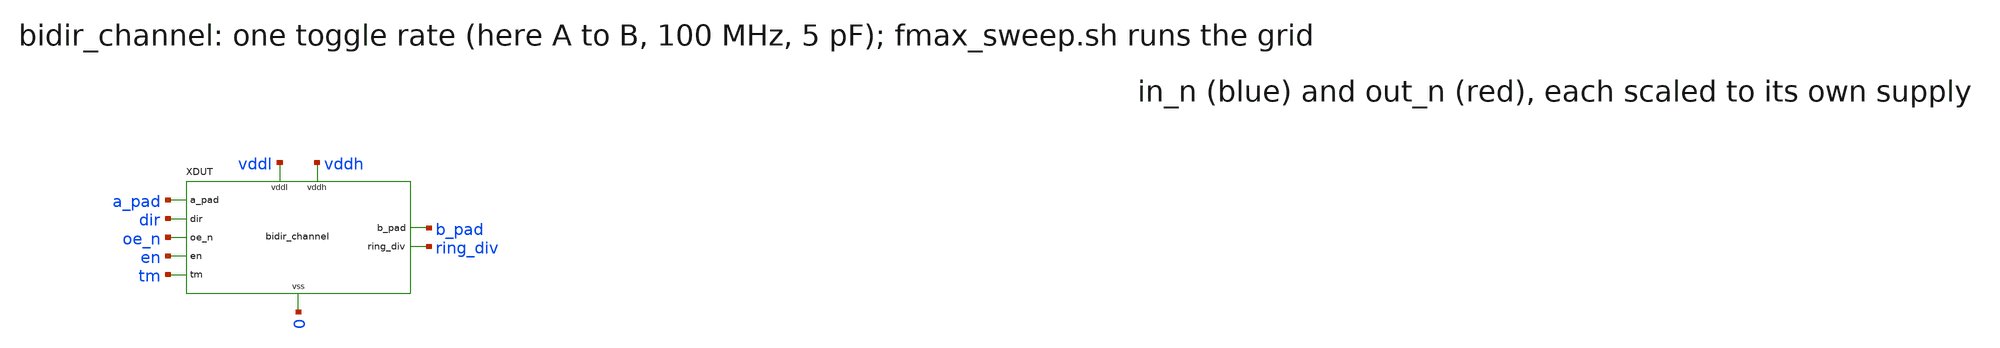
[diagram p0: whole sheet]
** sch_path: verification/tb_bidir_fmax.sch
**.subckt tb_bidir_fmax
XDUT a_pad b_pad dir oe_n en tm ring_div vddl vddh 0 bidir_channel
**** begin user architecture code

.lib cornerMOSlv.lib mos_tt
.lib cornerMOShv.lib mos_tt
.lib cornerRES.lib res_typ
VDL vddl 0 1.2
VDH vddh 0 3.3
Ven en 0 PWL(0 0 3n 0 3.5n 1.2)
Voe oe_n 0 0
Vtm tm 0 0
Vdir dir 0 0
Va adrv 0 PULSE(0 1.2 20n 0.1n 0.1n 4.9n 10n)
Vb bdrv 0 PULSE(0 3.3 20n 0.1n 0.1n 4.9n 10n)
* dir = 0: drive a_pad.  dir = 1: drive b_pad.  50 ohm source.
SA adrv a_pad vddl dir SWP
SB bdrv b_pad dir 0 SWP
.model SWP SW(Ron=50 Roff=1G Vt=0.6 Vh=0.05)
CA a_pad 0 5p
CB b_pad 0 5p
CR ring_div 0 1p
* driven pad and copying pad, both scaled to 0..1 of their own supply
Bin in_n 0 V = v(dir) < 0.6 ? v(a_pad)/v(vddl) : v(b_pad)/v(vddh)
Bout out_n 0 V = v(dir) < 0.6 ? v(b_pad)/v(vddh) : v(a_pad)/v(vddl)
.control
* One toggle rate, one direction, one pad load. fmax_sweep.sh edits these
* three lines and runs a grid of them.
let fr = 100e6
let cl = 5e-12
let dv = 0
* Pass: over periods 6-12 the output goes above 90 % and below 10 % of its
* supply and is high 40-60 % of the time.
option trtol=1
save a_pad b_pad in_n out_n
let vl = @vdl[dc]
let vh = @vdh[dc]
let per = 1 / fr
let pw = per / 2 - 0.1n
let t0 = 20n + 6 * per
let t1 = 20n + 12 * per
let ts = per / 200
alter @va[pulse] = [ 0 $&vl 20n 0.1n 0.1n $&pw $&per ]
alter @vb[pulse] = [ 0 $&vh 20n 0.1n 0.1n $&pw $&per ]
alter ca = $&cl
alter cb = $&cl
let vd = dv * vl
alter vdir dc = $&vd
tran $&ts $&t1
meas tran omax max v(out_n) from=$&t0 to=$&t1
meas tran omin min v(out_n) from=$&t0 to=$&t1
meas tran duty avg v(out_n) from=$&t0 to=$&t1
meas tran tplh trig v(in_n) val=0.5 rise=1 td=19n targ v(out_n) val=0.5 rise=1 td=19n
meas tran tphl trig v(in_n) val=0.5 fall=1 td=19n targ v(out_n) val=0.5 fall=1 td=19n
let pass = omax ge 0.9 and omin le 0.1 and duty ge 0.4 and duty le 0.6
echo result fr=$&fr cl=$&cl dir=$&dv pass=$&pass omax=$&omax omin=$&omin duty=$&duty tplh=$&tplh
+ tphl=$&tphl
write tb_bidir_fmax.raw
.endc

**** end user architecture code
**.ends
.end
